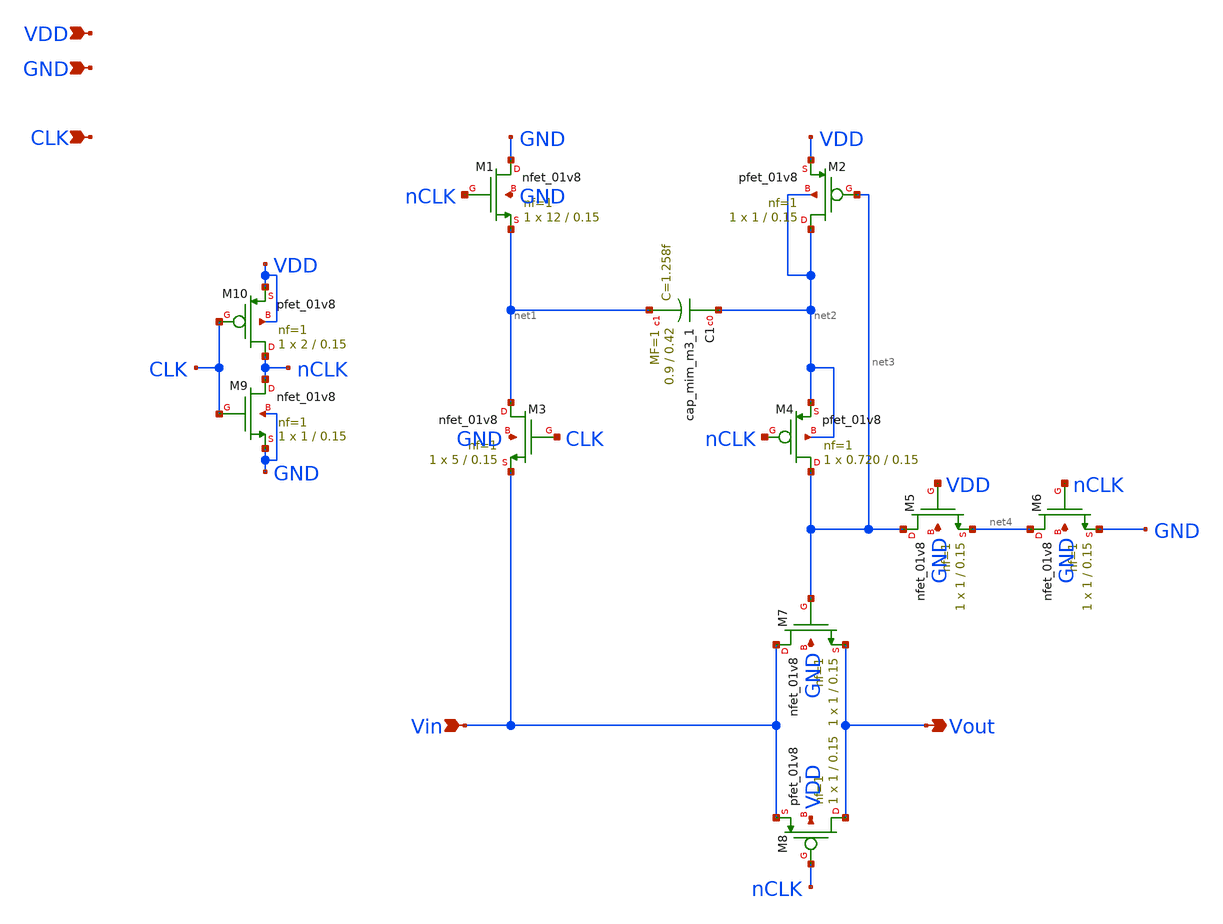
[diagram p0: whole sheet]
** sch_path: xschem/bootstrapedswitch.sch
**.subckt bootstrapedswitch VDD GND CLK Vout Vin
*.ipin VDD
*.ipin GND
*.ipin CLK
*.opin Vout
*.ipin Vin
XM1 GND nCLK net1 GND sky130_fd_pr__nfet_01v8 L=0.15 W=12 nf=1 ad='int((nf+1)/2) * W/nf * 0.29' as='int((nf+2)/2) * W/nf * 0.29'
+ pd='2*int((nf+1)/2) * (W/nf + 0.29)' ps='2*int((nf+2)/2) * (W/nf + 0.29)' nrd='0.29 / W' nrs='0.29 / W'
+ sa=0 sb=0 sd=0 mult=1 m=1
XM2 net2 net3 VDD net2 sky130_fd_pr__pfet_01v8 L=0.15 W=1 nf=1 ad='int((nf+1)/2) * W/nf * 0.29' as='int((nf+2)/2) * W/nf * 0.29'
+ pd='2*int((nf+1)/2) * (W/nf + 0.29)' ps='2*int((nf+2)/2) * (W/nf + 0.29)' nrd='0.29 / W' nrs='0.29 / W'
+ sa=0 sb=0 sd=0 mult=1 m=1
XC1 net2 net1 sky130_fd_pr__cap_mim_m3_1 W=0.9 L=0.42 MF=1 m=1
XM3 net1 CLK Vin GND sky130_fd_pr__nfet_01v8 L=0.15 W=5 nf=1 ad='int((nf+1)/2) * W/nf * 0.29' as='int((nf+2)/2) * W/nf * 0.29'
+ pd='2*int((nf+1)/2) * (W/nf + 0.29)' ps='2*int((nf+2)/2) * (W/nf + 0.29)' nrd='0.29 / W' nrs='0.29 / W'
+ sa=0 sb=0 sd=0 mult=1 m=1
XM4 net3 nCLK net2 net2 sky130_fd_pr__pfet_01v8 L=0.15 W=0.720 nf=1 ad='int((nf+1)/2) * W/nf * 0.29'
+ as='int((nf+2)/2) * W/nf * 0.29' pd='2*int((nf+1)/2) * (W/nf + 0.29)' ps='2*int((nf+2)/2) * (W/nf + 0.29)'
+ nrd='0.29 / W' nrs='0.29 / W' sa=0 sb=0 sd=0 mult=1 m=1
XM5 net3 VDD net4 GND sky130_fd_pr__nfet_01v8 L=0.15 W=1 nf=1 ad='int((nf+1)/2) * W/nf * 0.29' as='int((nf+2)/2) * W/nf * 0.29'
+ pd='2*int((nf+1)/2) * (W/nf + 0.29)' ps='2*int((nf+2)/2) * (W/nf + 0.29)' nrd='0.29 / W' nrs='0.29 / W'
+ sa=0 sb=0 sd=0 mult=1 m=1
XM6 net4 nCLK GND GND sky130_fd_pr__nfet_01v8 L=0.15 W=1 nf=1 ad='int((nf+1)/2) * W/nf * 0.29' as='int((nf+2)/2) * W/nf * 0.29'
+ pd='2*int((nf+1)/2) * (W/nf + 0.29)' ps='2*int((nf+2)/2) * (W/nf + 0.29)' nrd='0.29 / W' nrs='0.29 / W'
+ sa=0 sb=0 sd=0 mult=1 m=1
XM7 Vin net3 Vout GND sky130_fd_pr__nfet_01v8 L=0.15 W=1 nf=1 ad='int((nf+1)/2) * W/nf * 0.29' as='int((nf+2)/2) * W/nf * 0.29'
+ pd='2*int((nf+1)/2) * (W/nf + 0.29)' ps='2*int((nf+2)/2) * (W/nf + 0.29)' nrd='0.29 / W' nrs='0.29 / W'
+ sa=0 sb=0 sd=0 mult=1 m=1
XM8 Vout nCLK Vin VDD sky130_fd_pr__pfet_01v8 L=0.15 W=1 nf=1 ad='int((nf+1)/2) * W/nf * 0.29' as='int((nf+2)/2) * W/nf * 0.29'
+ pd='2*int((nf+1)/2) * (W/nf + 0.29)' ps='2*int((nf+2)/2) * (W/nf + 0.29)' nrd='0.29 / W' nrs='0.29 / W'
+ sa=0 sb=0 sd=0 mult=1 m=1
XM9 nCLK CLK GND GND sky130_fd_pr__nfet_01v8 L=0.15 W=1 nf=1 ad='int((nf+1)/2) * W/nf * 0.29' as='int((nf+2)/2) * W/nf * 0.29'
+ pd='2*int((nf+1)/2) * (W/nf + 0.29)' ps='2*int((nf+2)/2) * (W/nf + 0.29)' nrd='0.29 / W' nrs='0.29 / W'
+ sa=0 sb=0 sd=0 mult=1 m=1
XM10 nCLK CLK VDD VDD sky130_fd_pr__pfet_01v8 L=0.15 W=2 nf=1 ad='int((nf+1)/2) * W/nf * 0.29' as='int((nf+2)/2) * W/nf * 0.29'
+ pd='2*int((nf+1)/2) * (W/nf + 0.29)' ps='2*int((nf+2)/2) * (W/nf + 0.29)' nrd='0.29 / W' nrs='0.29 / W'
+ sa=0 sb=0 sd=0 mult=1 m=1
**.ends
.end
